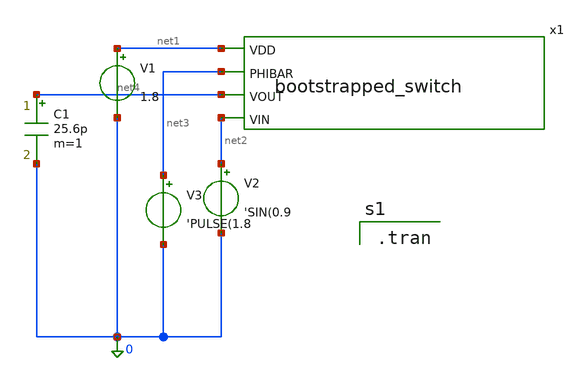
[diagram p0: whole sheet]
** sch_path: bootstrapped_switch_tb.sch
**.subckt bootstrapped_switch_tb
x1 net1 net3 net4 net2 bootstrapped_switch
V1 net1 0 1.8
V2 net2 0 'SIN(0.9
V3 net3 0 'PULSE(1.8
C1 net4 0 25.6p m=1
**** begin user architecture code

.tran

**** end user architecture code
**.ends

* expanding   symbol:  bootstrapped_switch.sym # of pins=4
** sym_path: bootstrapped_switch.sym
** sch_path: bootstrapped_switch.sch
.subckt bootstrapped_switch VDD PHIBAR VOUT VIN
*.ipin VDD
*.ipin VIN
*.ipin VOUT
*.ipin PHIBAR
XQ0 VIN net1 VOUT 0 sky130_fd_pr__nfet_01v8 L=0.15 W=1 nf=1 ad='int((nf+1)/2) * W/nf * 0.29' as='int((nf+2)/2) * W/nf * 0.29'
+ pd='2*int((nf+1)/2) * (W/nf + 0.29)' ps='2*int((nf+2)/2) * (W/nf + 0.29)' nrd='0.29 / W' nrs='0.29 / W'
+ sa=0 sb=0 sd=0 mult=1 m=1
XC_boot net3 net2 sky130_fd_pr__cap_mim_m3_1 W=15.6 L=15.6 MF=1 m=1
XQ5 net1 PHIBAR 0 0 sky130_fd_pr__nfet_01v8 L=0.15 W=1 nf=1 ad='int((nf+1)/2) * W/nf * 0.29' as='int((nf+2)/2) * W/nf * 0.29'
+ pd='2*int((nf+1)/2) * (W/nf + 0.29)' ps='2*int((nf+2)/2) * (W/nf + 0.29)' nrd='0.29 / W' nrs='0.29 / W'
+ sa=0 sb=0 sd=0 mult=1 m=1
XQ4 VIN net1 net2 0 sky130_fd_pr__nfet_01v8 L=0.15 W=1 nf=1 ad='int((nf+1)/2) * W/nf * 0.29' as='int((nf+2)/2) * W/nf * 0.29'
+ pd='2*int((nf+1)/2) * (W/nf + 0.29)' ps='2*int((nf+2)/2) * (W/nf + 0.29)' nrd='0.29 / W' nrs='0.29 / W'
+ sa=0 sb=0 sd=0 mult=1 m=1
XQ1 VDD net1 net3 net4 sky130_fd_pr__pfet_01v8 L=0.15 W=2 nf=1 ad='int((nf+1)/2) * W/nf * 0.29' as='int((nf+2)/2) * W/nf * 0.29'
+ pd='2*int((nf+1)/2) * (W/nf + 0.29)' ps='2*int((nf+2)/2) * (W/nf + 0.29)' nrd='0.29 / W' nrs='0.29 / W'
+ sa=0 sb=0 sd=0 mult=1 m=1
XQ3 net2 PHIBAR 0 0 sky130_fd_pr__nfet_01v8 L=0.15 W=1 nf=1 ad='int((nf+1)/2) * W/nf * 0.29' as='int((nf+2)/2) * W/nf * 0.29'
+ pd='2*int((nf+1)/2) * (W/nf + 0.29)' ps='2*int((nf+2)/2) * (W/nf + 0.29)' nrd='0.29 / W' nrs='0.29 / W'
+ sa=0 sb=0 sd=0 mult=1 m=1
XQ2 net3 PHIBAR net1 net4 sky130_fd_pr__pfet_01v8 L=0.15 W=1 nf=1 ad='int((nf+1)/2) * W/nf * 0.29' as='int((nf+2)/2) * W/nf * 0.29'
+ pd='2*int((nf+1)/2) * (W/nf + 0.29)' ps='2*int((nf+2)/2) * (W/nf + 0.29)' nrd='0.29 / W' nrs='0.29 / W'
+ sa=0 sb=0 sd=0 mult=1 m=1
XXWA net4 net1 VDD net4 sky130_fd_pr__pfet_01v8 L=0.15 W=1 nf=1 ad='int((nf+1)/2) * W/nf * 0.29' as='int((nf+2)/2) * W/nf * 0.29'
+ pd='2*int((nf+1)/2) * (W/nf + 0.29)' ps='2*int((nf+2)/2) * (W/nf + 0.29)' nrd='0.29 / W' nrs='0.29 / W'
+ sa=0 sb=0 sd=0 mult=1 m=1
XXWB net4 VDD net1 net4 sky130_fd_pr__pfet_01v8 L=0.15 W=1 nf=1 ad='int((nf+1)/2) * W/nf * 0.29' as='int((nf+2)/2) * W/nf * 0.29'
+ pd='2*int((nf+1)/2) * (W/nf + 0.29)' ps='2*int((nf+2)/2) * (W/nf + 0.29)' nrd='0.29 / W' nrs='0.29 / W'
+ sa=0 sb=0 sd=0 mult=1 m=1
.ends

.end
